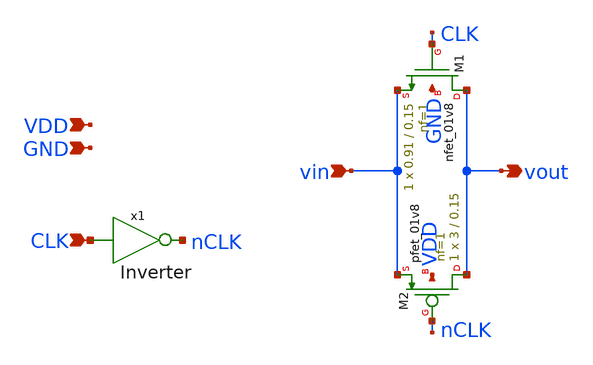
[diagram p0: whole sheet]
** sch_path: xschem/transgate.sch
**.subckt transgate VDD GND CLK vin vout
*.ipin VDD
*.ipin GND
*.ipin CLK
*.ipin vin
*.opin vout
XM1 vout CLK vin GND sky130_fd_pr__nfet_01v8 L=0.15 W=0.91 nf=1 ad='int((nf+1)/2) * W/nf * 0.29' as='int((nf+2)/2) * W/nf * 0.29'
+ pd='2*int((nf+1)/2) * (W/nf + 0.29)' ps='2*int((nf+2)/2) * (W/nf + 0.29)' nrd='0.29 / W' nrs='0.29 / W'
+ sa=0 sb=0 sd=0 mult=1 m=1
XM2 vout nCLK vin VDD sky130_fd_pr__pfet_01v8 L=0.15 W=3 nf=1 ad='int((nf+1)/2) * W/nf * 0.29' as='int((nf+2)/2) * W/nf * 0.29'
+ pd='2*int((nf+1)/2) * (W/nf + 0.29)' ps='2*int((nf+2)/2) * (W/nf + 0.29)' nrd='0.29 / W' nrs='0.29 / W'
+ sa=0 sb=0 sd=0 mult=1 m=1
x1 nCLK CLK Inverter
**.ends

* expanding   symbol:  Inverter.sym # of pins=2
** sym_path: xschem/Inverter.sym
** sch_path: xschem/Inverter.sch
.subckt Inverter Vout Vin
*.ipin Vin
*.opin Vout
XM1 Vout Vin GND GND sky130_fd_pr__nfet_01v8 L=0.15 W=1 nf=1 ad='int((nf+1)/2) * W/nf * 0.29' as='int((nf+2)/2) * W/nf * 0.29'
+ pd='2*int((nf+1)/2) * (W/nf + 0.29)' ps='2*int((nf+2)/2) * (W/nf + 0.29)' nrd='0.29 / W' nrs='0.29 / W'
+ sa=0 sb=0 sd=0 mult=1 m=1
XM2 Vout Vin VDD VDD sky130_fd_pr__pfet_01v8 L=0.15 W=4 nf=1 ad='int((nf+1)/2) * W/nf * 0.29' as='int((nf+2)/2) * W/nf * 0.29'
+ pd='2*int((nf+1)/2) * (W/nf + 0.29)' ps='2*int((nf+2)/2) * (W/nf + 0.29)' nrd='0.29 / W' nrs='0.29 / W'
+ sa=0 sb=0 sd=0 mult=1 m=1
V1 VDD GND 1.8
.ends

.GLOBAL GND
.end
